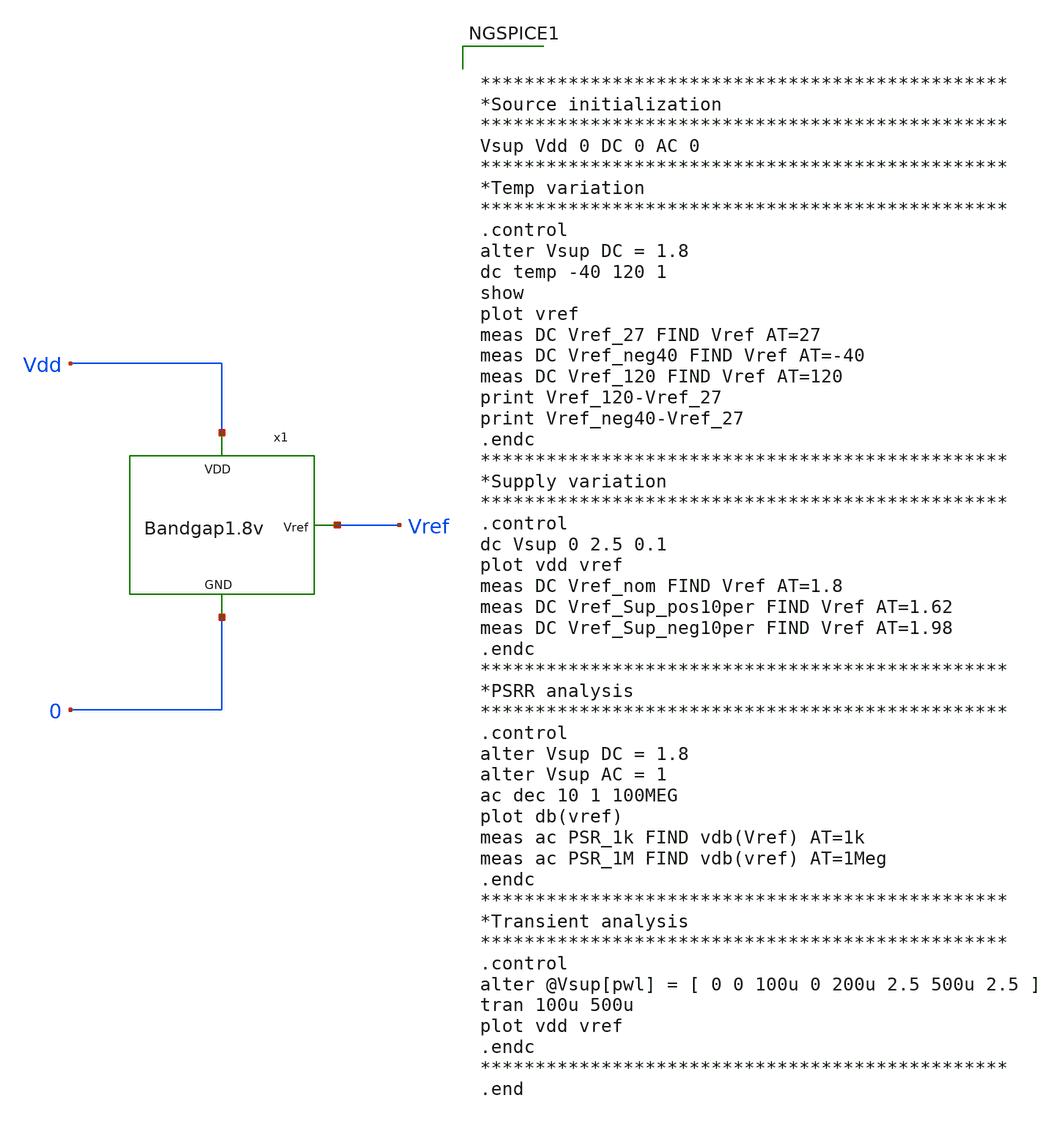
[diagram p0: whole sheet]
** sch_path: Analog_Blocks/Bandgap/Testbench/Bandgap1.8v_meas.sch
**.subckt Bandgap1.8v_meas
x1 Vref Vdd 0 Bandgap1.8v
**** begin user architecture code


************************************************
*Source initialization
************************************************
Vsup Vdd 0 DC 0 AC 0
************************************************
*Temp variation
************************************************
.control
alter Vsup DC = 1.8
dc temp -40 120 1
show
plot vref
meas DC Vref_27 FIND Vref AT=27
meas DC Vref_neg40 FIND Vref AT=-40
meas DC Vref_120 FIND Vref AT=120
print Vref_120-Vref_27
print Vref_neg40-Vref_27
.endc
************************************************
*Supply variation
************************************************
.control
dc Vsup 0 2.5 0.1
plot vdd vref
meas DC Vref_nom FIND Vref AT=1.8
meas DC Vref_Sup_pos10per FIND Vref AT=1.62
meas DC Vref_Sup_neg10per FIND Vref AT=1.98
.endc
************************************************
*PSRR analysis
************************************************
.control
alter Vsup DC = 1.8
alter Vsup AC = 1
ac dec 10 1 100MEG
plot db(vref)
meas ac PSR_1k FIND vdb(Vref) AT=1k
meas ac PSR_1M FIND vdb(vref) AT=1Meg
.endc
************************************************
*Transient analysis
************************************************
.control
alter @Vsup[pwl] = [ 0 0 100u 0 200u 2.5 500u 2.5 ]
tran 100u 500u
plot vdd vref
.endc
************************************************
.end




.param mc_mm_switch=0
.param mc_pr_switch=0
.include ~/mabrains/Analog_blocks/models/sky130A/libs.ref/sky130_fd_pr/spice/sky130_fd_pr__nfet_01v8__tt.corner.spice
.include ~/mabrains/Analog_blocks/models/sky130A/libs.ref/sky130_fd_pr/spice/sky130_fd_pr__nfet_01v8_lvt__tt.corner.spice
.include ~/mabrains/Analog_blocks/models/sky130A/libs.ref/sky130_fd_pr/spice/sky130_fd_pr__pfet_01v8__tt.corner.spice
.include ~/mabrains/Analog_blocks/models/sky130A/libs.ref/sky130_fd_pr/spice/sky130_fd_pr__nfet_03v3_nvt__tt.corner.spice
.include ~/mabrains/Analog_blocks/models/sky130A/libs.ref/sky130_fd_pr/spice/sky130_fd_pr__nfet_05v0_nvt__tt.corner.spice
.include ~/mabrains/Analog_blocks/models/sky130A/libs.ref/sky130_fd_pr/spice/sky130_fd_pr__esd_nfet_01v8__tt.corner.spice
.include ~/mabrains/Analog_blocks/models/sky130A/libs.ref/sky130_fd_pr/spice/sky130_fd_pr__pfet_01v8_lvt__tt.corner.spice
.include ~/mabrains/Analog_blocks/models/sky130A/libs.ref/sky130_fd_pr/spice/sky130_fd_pr__pfet_01v8_hvt__tt.corner.spice
.include ~/mabrains/Analog_blocks/models/sky130A/libs.ref/sky130_fd_pr/spice/sky130_fd_pr__esd_pfet_g5v0d10v5__tt.corner.spice
.include ~/mabrains/Analog_blocks/models/sky130A/libs.ref/sky130_fd_pr/spice/sky130_fd_pr__pfet_g5v0d10v5__tt.corner.spice
.include ~/mabrains/Analog_blocks/models/sky130A/libs.ref/sky130_fd_pr/spice/sky130_fd_pr__pfet_g5v0d16v0__tt.corner.spice
.include ~/mabrains/Analog_blocks/models/sky130A/libs.ref/sky130_fd_pr/spice/sky130_fd_pr__nfet_g5v0d10v5__tt.corner.spice
.include ~/mabrains/Analog_blocks/models/sky130A/libs.ref/sky130_fd_pr/spice/sky130_fd_pr__nfet_g5v0d16v0__tt_discrete.corner.spice
.include ~/mabrains/Analog_blocks/models/sky130A/libs.ref/sky130_fd_pr/spice/sky130_fd_pr__esd_nfet_g5v0d10v5__tt.corner.spice
.include ~/mabrains/Analog_blocks/models/sky130A/libs.tech/ngspice/corners/tt/nonfet.spice
* Mismatch parameters
.include ~/mabrains/Analog_blocks/models/sky130A/libs.ref/sky130_fd_pr/spice/sky130_fd_pr__nfet_01v8__mismatch.corner.spice
.include ~/mabrains/Analog_blocks/models/sky130A/libs.ref/sky130_fd_pr/spice/sky130_fd_pr__pfet_01v8__mismatch.corner.spice
.include ~/mabrains/Analog_blocks/models/sky130A/libs.ref/sky130_fd_pr/spice/sky130_fd_pr__nfet_01v8_lvt__mismatch.corner.spice
.include ~/mabrains/Analog_blocks/models/sky130A/libs.ref/sky130_fd_pr/spice/sky130_fd_pr__pfet_01v8_lvt__mismatch.corner.spice
.include ~/mabrains/Analog_blocks/models/sky130A/libs.ref/sky130_fd_pr/spice/sky130_fd_pr__pfet_01v8_hvt__mismatch.corner.spice
.include ~/mabrains/Analog_blocks/models/sky130A/libs.ref/sky130_fd_pr/spice/sky130_fd_pr__nfet_g5v0d10v5__mismatch.corner.spice
.include ~/mabrains/Analog_blocks/models/sky130A/libs.ref/sky130_fd_pr/spice/sky130_fd_pr__pfet_g5v0d10v5__mismatch.corner.spice
.include ~/mabrains/Analog_blocks/models/sky130A/libs.ref/sky130_fd_pr/spice/sky130_fd_pr__nfet_05v0_nvt__mismatch.corner.spice
.include ~/mabrains/Analog_blocks/models/sky130A/libs.ref/sky130_fd_pr/spice/sky130_fd_pr__nfet_03v3_nvt__mismatch.corner.spice
* Resistor/Capacitor
.include ~/mabrains/Analog_blocks/models/sky130A/libs.tech/ngspice/r+c/res_typical__cap_typical.spice
.include ~/mabrains/Analog_blocks/models/sky130A/libs.tech/ngspice/r+c/res_typical__cap_typical__lin.spice
* Special cells
.include ~/mabrains/Analog_blocks/models/sky130A/libs.tech/ngspice/corners/tt/specialized_cells.spice
* All models
.include ~/mabrains/Analog_blocks/models/sky130A/libs.tech/ngspice/all.spice
* Corner
.include ~/mabrains/Analog_blocks/models/sky130A/libs.tech/ngspice/corners/tt/rf.spice



**** end user architecture code
**.ends
.end
